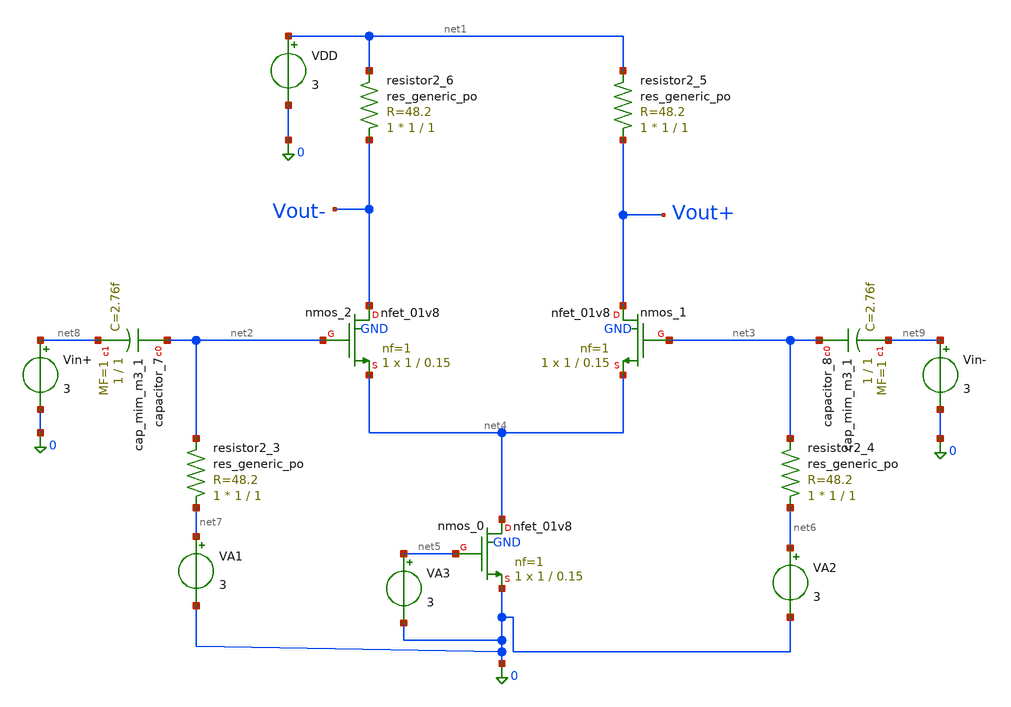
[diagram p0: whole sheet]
** sch_path: golden_netlists/10_1109_ACCESS_2021_3064007_05_001.sch
**.subckt 10_1109_ACCESS_2021_3064007_05_001
Xcapacitor_7 net2 net8 sky130_fd_pr__cap_mim_m3_1 W=1 L=1 MF=1 m=1
Xcapacitor_8 net3 net9 sky130_fd_pr__cap_mim_m3_1 W=1 L=1 MF=1 m=1
Xnmos_0 net4 net5 0 GND sky130_fd_pr__nfet_01v8 L=0.15 W=1 nf=1 ad='int((nf+1)/2) * W/nf * 0.29' as='int((nf+2)/2) * W/nf * 0.29'
+ pd='2*int((nf+1)/2) * (W/nf + 0.29)' ps='2*int((nf+2)/2) * (W/nf + 0.29)' nrd='0.29 / W' nrs='0.29 / W'
+ sa=0 sb=0 sd=0 mult=1 m=1
Xnmos_1 Vout+ net3 net4 GND sky130_fd_pr__nfet_01v8 L=0.15 W=1 nf=1 ad='int((nf+1)/2) * W/nf * 0.29'
+ as='int((nf+2)/2) * W/nf * 0.29' pd='2*int((nf+1)/2) * (W/nf + 0.29)' ps='2*int((nf+2)/2) * (W/nf + 0.29)'
+ nrd='0.29 / W' nrs='0.29 / W' sa=0 sb=0 sd=0 mult=1 m=1
Xnmos_2 Vout- net2 net4 GND sky130_fd_pr__nfet_01v8 L=0.15 W=1 nf=1 ad='int((nf+1)/2) * W/nf * 0.29'
+ as='int((nf+2)/2) * W/nf * 0.29' pd='2*int((nf+1)/2) * (W/nf + 0.29)' ps='2*int((nf+2)/2) * (W/nf + 0.29)'
+ nrd='0.29 / W' nrs='0.29 / W' sa=0 sb=0 sd=0 mult=1 m=1
Xresistor2_3 net7 net2 sky130_fd_pr__res_generic_po W=1 L=1 m=1
Xresistor2_4 net6 net3 sky130_fd_pr__res_generic_po W=1 L=1 m=1
Xresistor2_5 Vout+ net1 sky130_fd_pr__res_generic_po W=1 L=1 m=1
Xresistor2_6 Vout- net1 sky130_fd_pr__res_generic_po W=1 L=1 m=1
VDD net1 0 3
VA3 net5 0 3
VA1 net7 0 3
VA2 net6 0 3
Vin+ net8 0 3
Vin- net9 0 3
**.ends
.end
